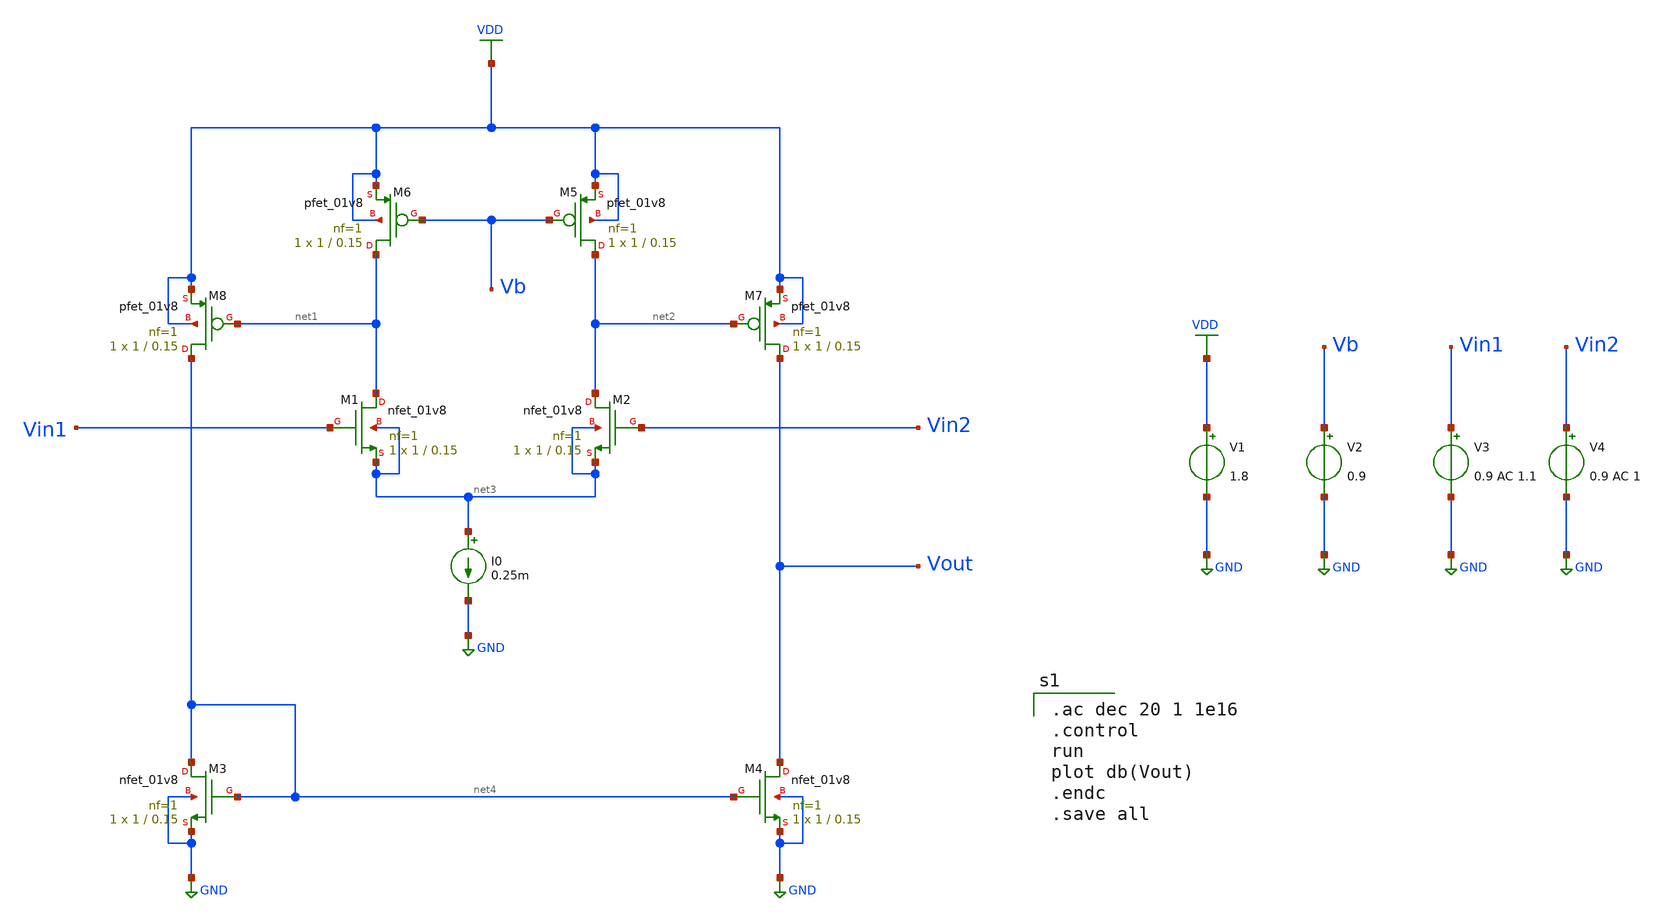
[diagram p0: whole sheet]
** sch_path: Circuits/Examples/Analog/Op_Amp/single_end_opamp.sch
**.subckt single_end_opamp
XM1 net1 Vin1 net3 net3 sky130_fd_pr__nfet_01v8 L=0.15 W=1 nf=1 ad='int((nf+1)/2) * W/nf * 0.29' as='int((nf+2)/2) * W/nf * 0.29'
+ pd='2*int((nf+1)/2) * (W/nf + 0.29)' ps='2*int((nf+2)/2) * (W/nf + 0.29)' nrd='0.29 / W' nrs='0.29 / W'
+ sa=0 sb=0 sd=0 mult=1 m=1
XM4 Vout net4 GND GND sky130_fd_pr__nfet_01v8 L=0.15 W=1 nf=1 ad='int((nf+1)/2) * W/nf * 0.29' as='int((nf+2)/2) * W/nf * 0.29'
+ pd='2*int((nf+1)/2) * (W/nf + 0.29)' ps='2*int((nf+2)/2) * (W/nf + 0.29)' nrd='0.29 / W' nrs='0.29 / W'
+ sa=0 sb=0 sd=0 mult=1 m=1
XM5 net2 Vb VDD VDD sky130_fd_pr__pfet_01v8 L=0.15 W=1 nf=1 ad='int((nf+1)/2) * W/nf * 0.29' as='int((nf+2)/2) * W/nf * 0.29'
+ pd='2*int((nf+1)/2) * (W/nf + 0.29)' ps='2*int((nf+2)/2) * (W/nf + 0.29)' nrd='0.29 / W' nrs='0.29 / W'
+ sa=0 sb=0 sd=0 mult=1 m=1
XM7 Vout net2 VDD VDD sky130_fd_pr__pfet_01v8 L=0.15 W=1 nf=1 ad='int((nf+1)/2) * W/nf * 0.29' as='int((nf+2)/2) * W/nf * 0.29'
+ pd='2*int((nf+1)/2) * (W/nf + 0.29)' ps='2*int((nf+2)/2) * (W/nf + 0.29)' nrd='0.29 / W' nrs='0.29 / W'
+ sa=0 sb=0 sd=0 mult=1 m=1
I0 net3 GND 0.25m
V1 VDD GND 1.8
V2 Vb GND 0.9
V3 Vin1 GND 0.9 AC 1.1
V4 Vin2 GND 0.9 AC 1
XM2 net2 Vin2 net3 net3 sky130_fd_pr__nfet_01v8 L=0.15 W=1 nf=1 ad='int((nf+1)/2) * W/nf * 0.29' as='int((nf+2)/2) * W/nf * 0.29'
+ pd='2*int((nf+1)/2) * (W/nf + 0.29)' ps='2*int((nf+2)/2) * (W/nf + 0.29)' nrd='0.29 / W' nrs='0.29 / W'
+ sa=0 sb=0 sd=0 mult=1 m=1
XM6 net1 Vb VDD VDD sky130_fd_pr__pfet_01v8 L=0.15 W=1 nf=1 ad='int((nf+1)/2) * W/nf * 0.29' as='int((nf+2)/2) * W/nf * 0.29'
+ pd='2*int((nf+1)/2) * (W/nf + 0.29)' ps='2*int((nf+2)/2) * (W/nf + 0.29)' nrd='0.29 / W' nrs='0.29 / W'
+ sa=0 sb=0 sd=0 mult=1 m=1
XM8 net4 net1 VDD VDD sky130_fd_pr__pfet_01v8 L=0.15 W=1 nf=1 ad='int((nf+1)/2) * W/nf * 0.29' as='int((nf+2)/2) * W/nf * 0.29'
+ pd='2*int((nf+1)/2) * (W/nf + 0.29)' ps='2*int((nf+2)/2) * (W/nf + 0.29)' nrd='0.29 / W' nrs='0.29 / W'
+ sa=0 sb=0 sd=0 mult=1 m=1
XM3 net4 net4 GND GND sky130_fd_pr__nfet_01v8 L=0.15 W=1 nf=1 ad='int((nf+1)/2) * W/nf * 0.29' as='int((nf+2)/2) * W/nf * 0.29'
+ pd='2*int((nf+1)/2) * (W/nf + 0.29)' ps='2*int((nf+2)/2) * (W/nf + 0.29)' nrd='0.29 / W' nrs='0.29 / W'
+ sa=0 sb=0 sd=0 mult=1 m=1
**** begin user architecture code
 ** manual skywater pdks install (with patches applied)
* .lib $::SKYWATER_MODELS/models/sky130.lib.spice tt

** opencircuitdesign pdks install
.lib $::SKYWATER_MODELS/sky130.lib.spice tt

.param mc_mm_switch=0
.param mc_pr_switch=0


.ac dec 20 1 1e16
.control
run
plot db(Vout)
.endc
.save all

**** end user architecture code
**.ends
.GLOBAL GND
.GLOBAL VDD
.end
